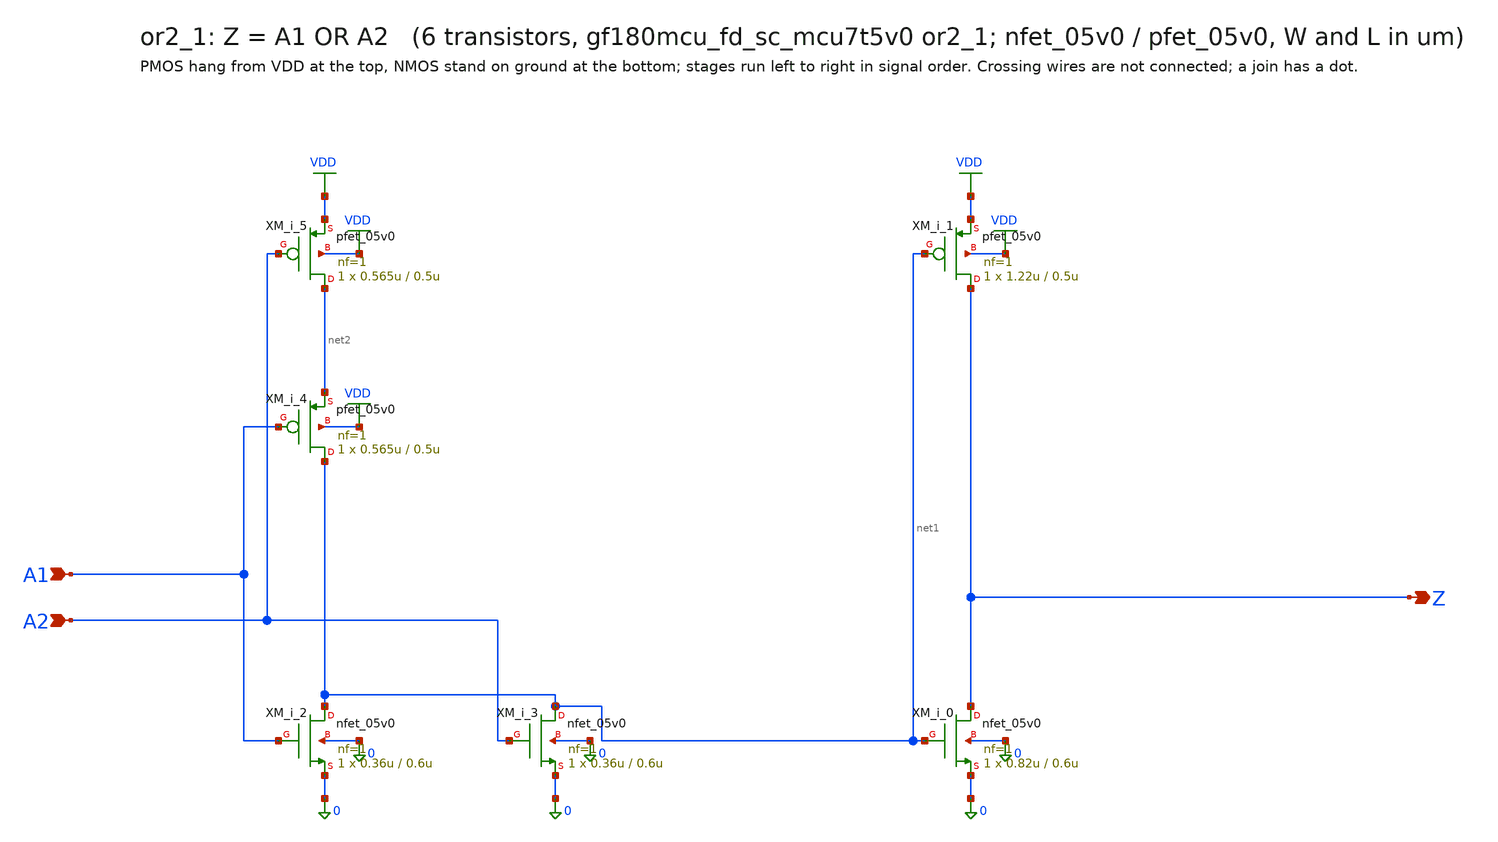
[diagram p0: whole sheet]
** sch_path: xschem/cells_tx/or2_1.sch
**.subckt or2_1 A1 A2 Z
*.ipin A1
*.ipin A2
*.opin Z
XM_i_2 net1 A1 0 0 nfet_05v0 L=0.6u W=0.36u nf=1 ad=1.8e-13 as=1.8e-13 pd=1.72e-06 ps=1.72e-06 nrd=0
+ nrs=0 sa=0 sb=0 sd=0 m=1
XM_i_3 net1 A2 0 0 nfet_05v0 L=0.6u W=0.36u nf=1 ad=1.8e-13 as=1.8e-13 pd=1.72e-06 ps=1.72e-06 nrd=0
+ nrs=0 sa=0 sb=0 sd=0 m=1
XM_i_0 Z net1 0 0 nfet_05v0 L=0.6u W=0.82u nf=1 ad=4.1e-13 as=4.1e-13 pd=2.64e-06 ps=2.64e-06 nrd=0
+ nrs=0 sa=0 sb=0 sd=0 m=1
XM_i_4 net1 A1 net2 VDD pfet_05v0 L=0.5u W=0.565u nf=1 ad=2.825e-13 as=2.825e-13 pd=2.13e-06
+ ps=2.13e-06 nrd=0 nrs=0 sa=0 sb=0 sd=0 m=1
XM_i_5 net2 A2 VDD VDD pfet_05v0 L=0.5u W=0.565u nf=1 ad=2.825e-13 as=2.825e-13 pd=2.13e-06
+ ps=2.13e-06 nrd=0 nrs=0 sa=0 sb=0 sd=0 m=1
XM_i_1 Z net1 VDD VDD pfet_05v0 L=0.5u W=1.22u nf=1 ad=6.1e-13 as=6.1e-13 pd=3.44e-06 ps=3.44e-06
+ nrd=0 nrs=0 sa=0 sb=0 sd=0 m=1
**.ends
.GLOBAL VDD
.end
